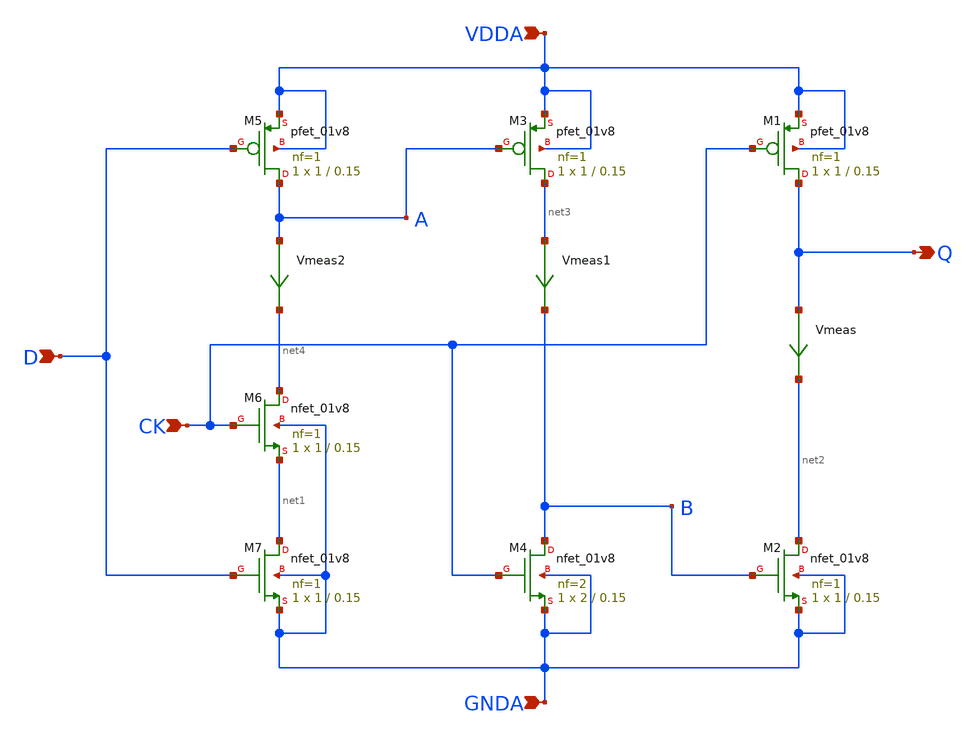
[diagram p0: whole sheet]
** sch_path: projects/pll/divider/xschem_ngspice/TSPC_FF_ratioed.sch
**.subckt TSPC_FF_ratioed CK D Q VDDA GNDA
*.ipin CK
*.ipin D
*.opin Q
*.ipin VDDA
*.ipin GNDA
XM1 Q CK VDDA VDDA sky130_fd_pr__pfet_01v8 L=0.15 W=1 nf=1 ad='int((nf+1)/2) * W/nf * 0.29' as='int((nf+2)/2) * W/nf * 0.29'
+ pd='2*int((nf+1)/2) * (W/nf + 0.29)' ps='2*int((nf+2)/2) * (W/nf + 0.29)' nrd='0.29 / W' nrs='0.29 / W'
+ sa=0 sb=0 sd=0 mult=1 m=1
Vmeas Q net2 0
.save i(vmeas)
XM2 net2 B GNDA GNDA sky130_fd_pr__nfet_01v8 L=0.15 W=1 nf=1 ad='int((nf+1)/2) * W/nf * 0.29' as='int((nf+2)/2) * W/nf * 0.29'
+ pd='2*int((nf+1)/2) * (W/nf + 0.29)' ps='2*int((nf+2)/2) * (W/nf + 0.29)' nrd='0.29 / W' nrs='0.29 / W'
+ sa=0 sb=0 sd=0 mult=1 m=1
XM3 net3 A VDDA VDDA sky130_fd_pr__pfet_01v8 L=0.15 W=1 nf=1 ad='int((nf+1)/2) * W/nf * 0.29' as='int((nf+2)/2) * W/nf * 0.29'
+ pd='2*int((nf+1)/2) * (W/nf + 0.29)' ps='2*int((nf+2)/2) * (W/nf + 0.29)' nrd='0.29 / W' nrs='0.29 / W'
+ sa=0 sb=0 sd=0 mult=1 m=1
XM4 B CK GNDA GNDA sky130_fd_pr__nfet_01v8 L=0.15 W=2 nf=2 ad='int((nf+1)/2) * W/nf * 0.29' as='int((nf+2)/2) * W/nf * 0.29'
+ pd='2*int((nf+1)/2) * (W/nf + 0.29)' ps='2*int((nf+2)/2) * (W/nf + 0.29)' nrd='0.29 / W' nrs='0.29 / W'
+ sa=0 sb=0 sd=0 mult=1 m=1
Vmeas1 net3 B 0
.save i(vmeas1)
XM5 A D VDDA VDDA sky130_fd_pr__pfet_01v8 L=0.15 W=1 nf=1 ad='int((nf+1)/2) * W/nf * 0.29' as='int((nf+2)/2) * W/nf * 0.29'
+ pd='2*int((nf+1)/2) * (W/nf + 0.29)' ps='2*int((nf+2)/2) * (W/nf + 0.29)' nrd='0.29 / W' nrs='0.29 / W'
+ sa=0 sb=0 sd=0 mult=1 m=1
XM7 net1 D GNDA GNDA sky130_fd_pr__nfet_01v8 L=0.15 W=1 nf=1 ad='int((nf+1)/2) * W/nf * 0.29' as='int((nf+2)/2) * W/nf * 0.29'
+ pd='2*int((nf+1)/2) * (W/nf + 0.29)' ps='2*int((nf+2)/2) * (W/nf + 0.29)' nrd='0.29 / W' nrs='0.29 / W'
+ sa=0 sb=0 sd=0 mult=1 m=1
Vmeas2 A net4 0
.save i(vmeas2)
XM6 net4 CK net1 GNDA sky130_fd_pr__nfet_01v8 L=0.15 W=1 nf=1 ad='int((nf+1)/2) * W/nf * 0.29' as='int((nf+2)/2) * W/nf * 0.29'
+ pd='2*int((nf+1)/2) * (W/nf + 0.29)' ps='2*int((nf+2)/2) * (W/nf + 0.29)' nrd='0.29 / W' nrs='0.29 / W'
+ sa=0 sb=0 sd=0 mult=1 m=1
**.ends
.end
